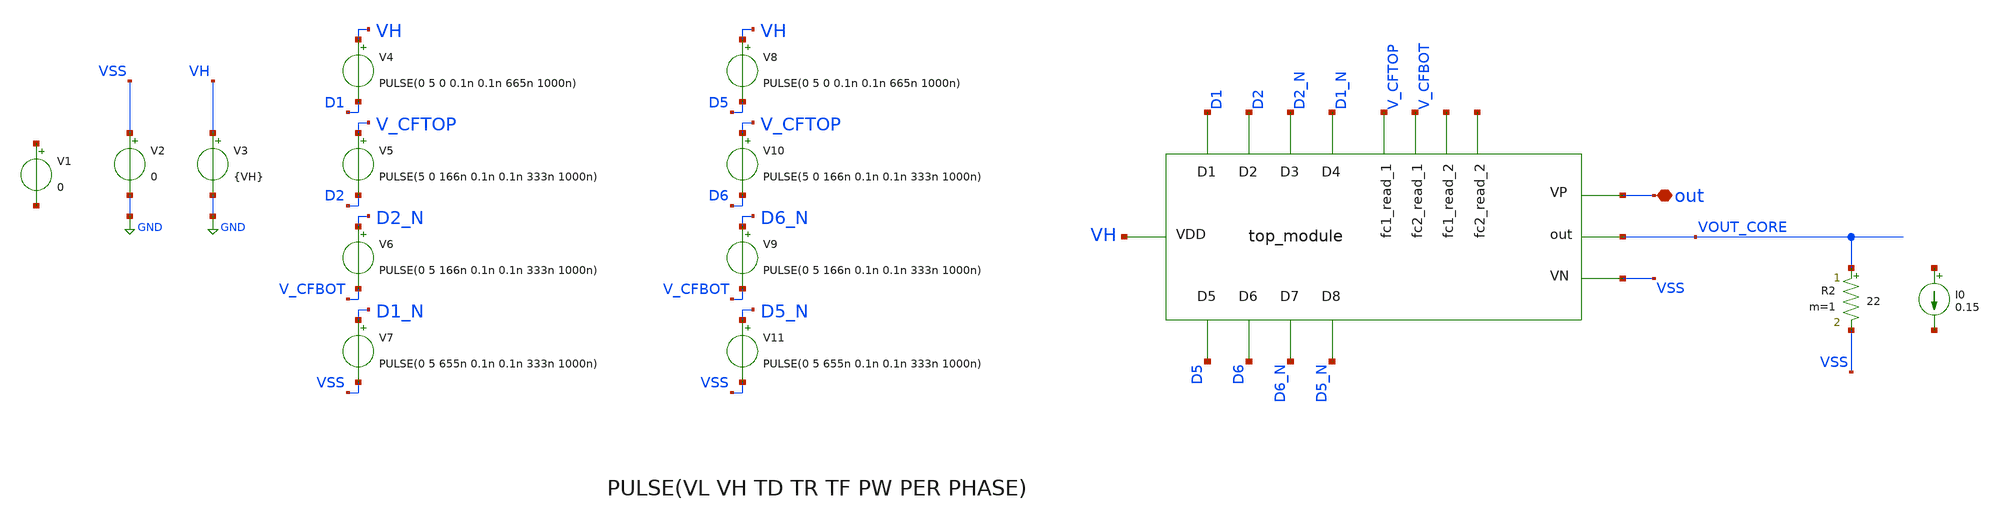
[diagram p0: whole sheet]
** sch_path: xschem/testbench/TopModule/top_module_testbench.sch
**.subckt top_module_testbench out
*.iopin out
V4 VH D1 PULSE(0 5 0 0.1n 0.1n 665n 1000n)
V2 VSS GND 0
V6 D2_N V_CFBOT PULSE(0 5 166n 0.1n 0.1n 333n 1000n)
V3 VH GND {VH}
V5 V_CFTOP D2 PULSE(5 0 166n 0.1n 0.1n 333n 1000n)
V7 D1_N VSS PULSE(0 5 655n 0.1n 0.1n 333n 1000n)
I0 net1 net2 0.15
R2 VOUT_CORE VSS 22 m=1
X2 D5 D6 D6_N D5_N VSS VOUT_CORE out D1 D2 D2_N D1_N VH V_CFTOP V_CFBOT net3 net4 top_module
V1 net5 net6 0
V8 VH D5 PULSE(0 5 0 0.1n 0.1n 665n 1000n)
V9 D6_N V_CFBOT PULSE(0 5 166n 0.1n 0.1n 333n 1000n)
V10 V_CFTOP D6 PULSE(5 0 166n 0.1n 0.1n 333n 1000n)
V11 D5_N VSS PULSE(0 5 655n 0.1n 0.1n 333n 1000n)
**** begin user architecture code


.param VIN = 5
.param VH = 5
.param RL = 50
.option scale=1e-6
*.option temp=70
.ic v(V_CFTOP) = VH/2
.ic v(vout)=0
.ic v(V_CFBOT) = 0
*.probe vd(MP2:G:S)
*.save all
*.save v(d1) v(d2) v(d1top_5v) v(d2_5v) v(d2bot_5v) v(d1bot_5v) v(vout) v(vout_core) v(vdd) v(vh) i(v1) i(v5) i(vmeas) v(v_cftop,v_cfbot)
.save v(D1) v(D2) v(D1_N) v(D2_N) v(VOUT) v(VOUT_CORE) v(vdd) v(vh) i(v3) i(vmeas) v(v_cftop,v_cfbot) v(D1,v_cftop) v(D2,vout_core) v(D2_N,v_cfbot) v(D1_Nv,VSS)
.save @m.xm4.msky130_fd_pr__nfet_g5v0d10v5[vds]
.param mc_mm_switch=0
*.lib /home/jorge/Documents/Postdoc/share/pdk/sky130A/libs.tech/ngspice/sky130.lib.spice tt
*.lib /usr/share/pdk/sky130A/libs.tech/ngspice/sky130.lib.spice ss
.lib /foss/pdk/sky130A/libs.tech/ngspice/sky130.lib.spice TT
*.include /usr/share/pdk/sky130A/libs.ref/sky130_fd_sc_hvl/spice/sky130_fd_sc_hvl.spice
*.include /home/jorge/Documents/Postdoc/share/pdk/sky130A/libs.ref/sky130_fd_sc_hvl/spice/sky130_fd_sc_hvl.spice
.options savecurrents
.control
*save all
tran 400n 3u
write DCDC_v1p4_5MHz_NMOS_PMOS.raw
*wrdata
*+ ~/Documents/Postdoc/chipathon2022/3LFCC_AC3E/xschem/dev_switches/DCDC_5V_FINAL/3LFCC_v1p4.txt tran.v(vout) tran.i(vmeas) tran.v(vdd) tran.i(v3) tran.v(vh) tran.i(v5)
wrdata /foss/designs/personal/3LFCC_AC3E/xschem/hierarchy_sch/DCDC_5V_FINAL/3LFCC_v1p4.txt
+ tran.v(vout) tran.i(v3)

*plot v(d1top_5v) v(d2_5v)
*plot v(d2bot_5v) v(d1bot_5v)
plot v(v_cftop,v_cfbot) v(vout_core)
plot v(D1,VH) v(D1_N,VSS)
plot v(D2,V_CFTOP) v(D2_N,V_CFBOT)
plot  v(vout_core)
plot i(v3) v(D1,VH) v(D2,V_CFTOP)
plot i(v3) v(D1_N,VSS) v(D2_N,V_CFBOT)
plot i(v3)
plot i(v3) v(v_cftop,v_cfbot)
plot @m.xm4.msky130_fd_pr__nfet_g5v0d10v5[vds]


*plot v(d1top_5v) v(d2_5v) v(d2bot_5v) v(d1bot_5v) v(v_cftop,v_cfbot) v(vout)
*plot v(v_cftop,v_cfbot) v(vout)
.endc


**** end user architecture code
**.ends
.GLOBAL GND
.end
